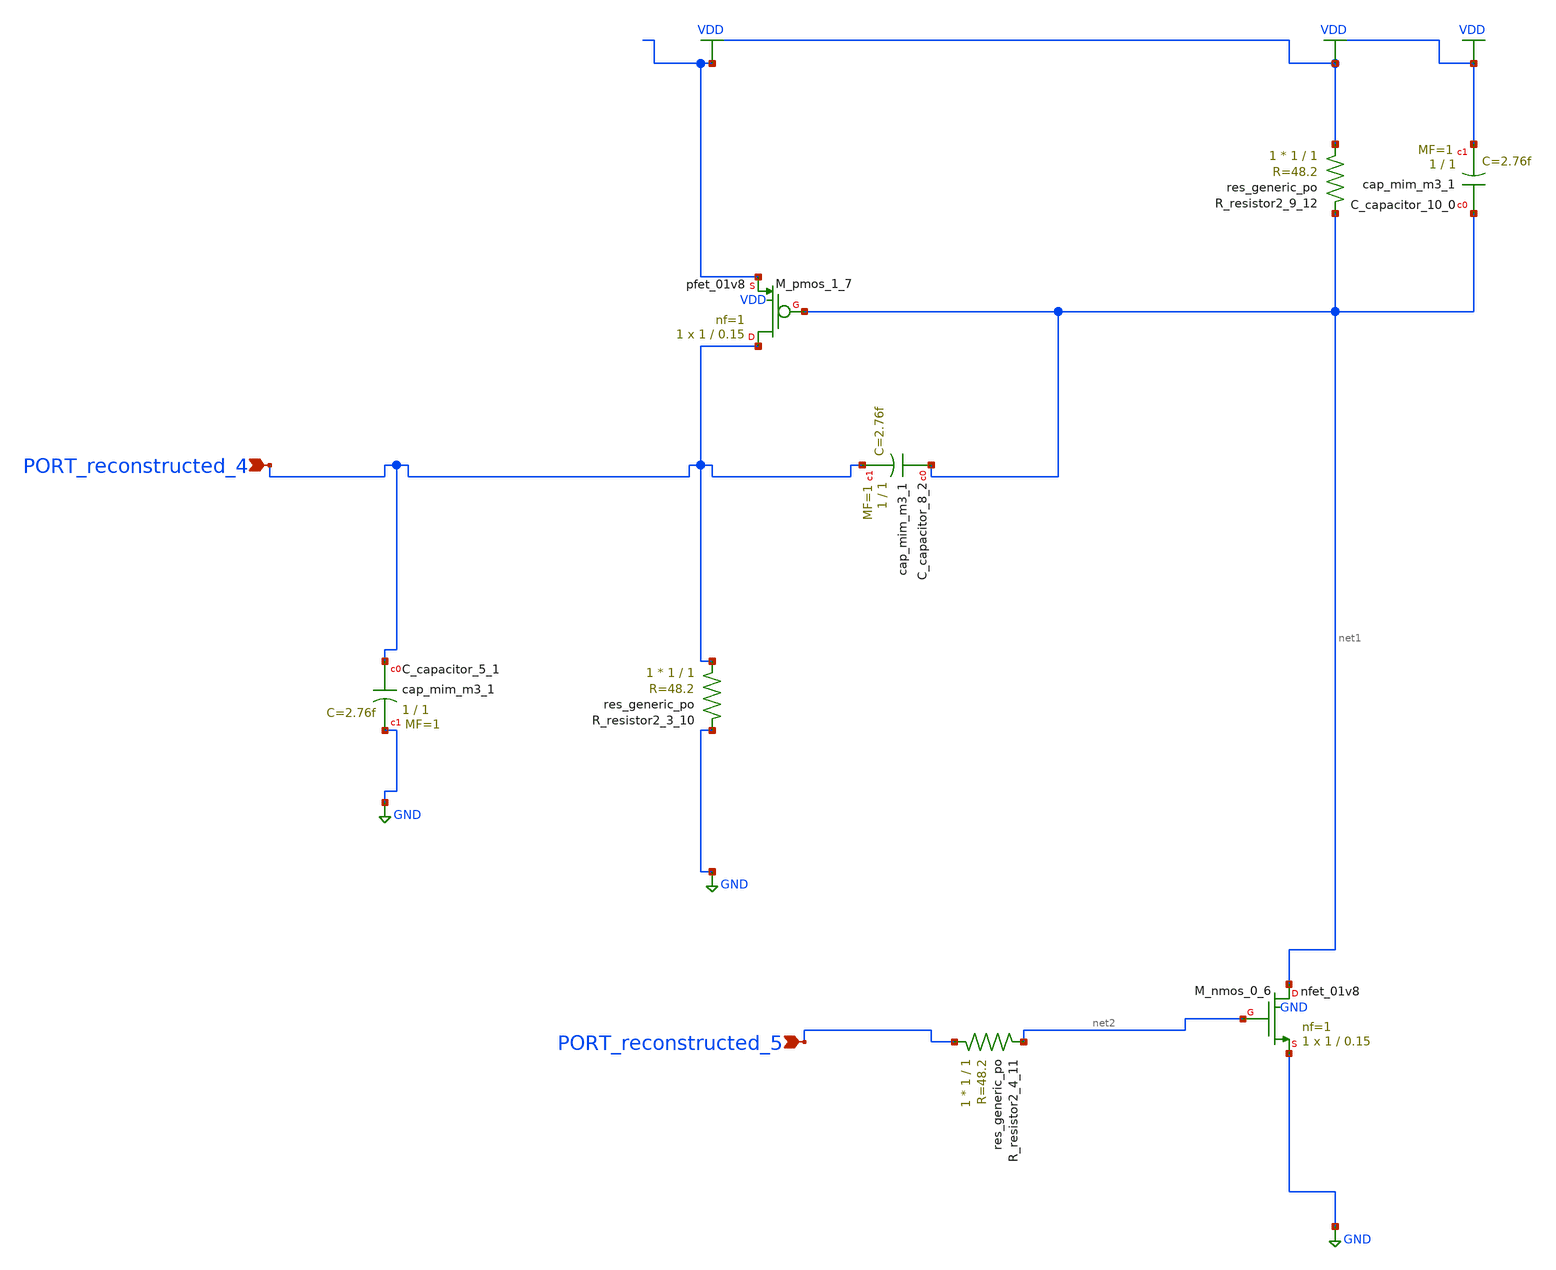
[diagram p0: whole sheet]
** sch_path: schematics/AMSNet/394.sch
**.subckt 394 PORT_reconstructed_4 PORT_reconstructed_5
*.ipin PORT_reconstructed_4
*.ipin PORT_reconstructed_5
XC_capacitor_10_0 net1 VDD sky130_fd_pr__cap_mim_m3_1 W=1 L=1 MF=1 m=1
XC_capacitor_5_1 PORT_reconstructed_4 GND sky130_fd_pr__cap_mim_m3_1 W=1 L=1 MF=1 m=1
XC_capacitor_8_2 net1 PORT_reconstructed_4 sky130_fd_pr__cap_mim_m3_1 W=1 L=1 MF=1 m=1
XM_nmos_0_6 net1 net2 GND GND sky130_fd_pr__nfet_01v8 L=0.15 W=1 nf=1 ad='int((1 + 1)/2) * 1 / 1 * 0.29'
+ as='int((1 + 2)/2) * 1 / 1 * 0.29' pd='2*int((1 + 1)/2) * (1 / 1 + 0.29)' ps='2*int((1 + 2)/2) * (1 / 1 + 0.29)'
+ nrd='0.29 / 1 ' nrs='0.29 / 1 ' sa=0 sb=0 sd=0 mult=1 m=1
XM_pmos_1_7 PORT_reconstructed_4 net1 VDD VDD sky130_fd_pr__pfet_01v8 L=0.15 W=1 nf=1 ad='int((1 + 1)/2) * 1 / 1 * 0.29'
+ as='int((1 + 2)/2) * 1 / 1 * 0.29' pd='2*int((1 + 1)/2) * (1 / 1 + 0.29)' ps='2*int((1 + 2)/2) * (1 / 1 + 0.29)'
+ nrd='0.29 / 1 ' nrs='0.29 / 1 ' sa=0 sb=0 sd=0 mult=1 m=1
XR_resistor2_3_10 PORT_reconstructed_4 GND sky130_fd_pr__res_generic_po W=1 L=1 m=1
XR_resistor2_4_11 PORT_reconstructed_5 net2 sky130_fd_pr__res_generic_po W=1 L=1 m=1
XR_resistor2_9_12 VDD net1 sky130_fd_pr__res_generic_po W=1 L=1 m=1
**.ends
.GLOBAL GND
.GLOBAL VDD
.end
